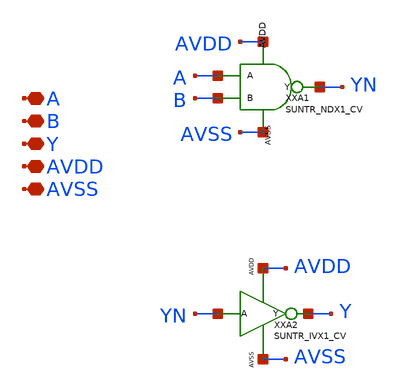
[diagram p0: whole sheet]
** sch_path: design/SUN_TR_SKY130NM/SUNTR_ANX4_CV.sch
**.subckt SUNTR_ANX4_CV A B Y AVDD AVSS
*.iopin A
*.iopin B
*.iopin Y
*.iopin AVDD
*.iopin AVSS
XXA1 A B YN AVDD AVSS SUNTR_NDX1_CV
XXA2 YN Y AVDD AVSS SUNTR_IVX1_CV
**.ends
.end
